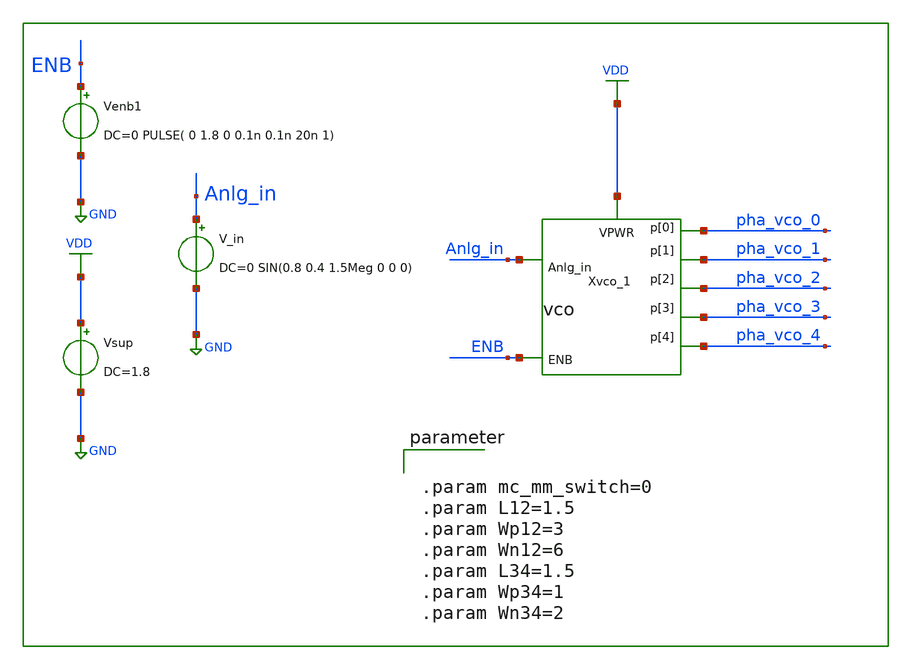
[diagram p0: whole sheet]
** sch_path: circuit_model/tb/vco.sch
**.subckt vco
Vsup VDD GND DC=1.8
V_in Anlg_in GND DC=0 SIN(0.8 0.4 1.5Meg 0 0 0)
Venb1 ENB GND DC=0 PULSE( 0 1.8 0 0.1n 0.1n 20n 1)
Xvco_1 VDD pha_vco_0 pha_vco_1 pha_vco_2 pha_vco_3 pha_vco_4 Anlg_in ENB vco L12="L12" Wp12="Wp12"
+ Wn12="Wn12" L34="L34" Wp34="Wp34" Wn34="Wn34"
**** begin user architecture code


.control
set nobreak
set num_threads=11
set test_mode = 0
* mode = 0: operation testing				1:  frequency extraction    2:  power consumption
if ($test_mode = 0)
    TRAN 1n 10u
    plot Anlg_in pha_vco_0
    MEAS TRAN prd_0 TRIG pha_vco_0 VAL=0.8 RISE=10 TARG pha_vco_0 VAL=0.8 RISE=20
    let freq_0 = 10/prd_0
    echo "frequency: "
    print freq_0
end

if ($test_mode = 1)
    let Vlow = 0
    let Vlimit = 1.01     $ set upper bound for sweeping
    let Vsweep = 0.2      $ set step size for sweeping
    let NoPoints=(Vlimit-Vlow)/Vsweep+2    $ set number of points for sweeping
    let freq_0 =unitvec(NoPoints)
    let Vin  =unitvec(NoPoints)
    let Vin[0]=Vlow
    let ix=0
    let I_vco =unitvec(NoPoints)
    while Vin[ix] < Vlimit
        alter V_in DC=Vin[ix]
        TRAN 1n 	10u
	SAVE @R_debug[i] pha_vco_0
        MEAS TRAN prd_0 TRIG pha_vco_0 VAL=0.8 RISE=10 TARG pha_vco_0 VAL=0.8 RISE =20
	MEAS TRAN Ivco 0 AVG @R_debug[i] FROM=1u TO=6u
	let I_vco[ix] = Ivco
        let freq_0[ix] = 10/prd_0
        let ix = ix+1
        Let Vin[ix] = Vin[ix-1]+Vsweep
    end
   print Vin freq_0 I_vco
end

if ($test_mode = 2)
    save "vdd" @Vsup[i] "p[0]"
    TRAN 1n 6u
    MEAS TRAN I_vco AVG @Vsup[i] FROM=3u TO=4u
    MEAS TRAN V_vco AVG vdd FROM=3u TO=4u
    let Power=I_vco*V_vco
    print Power
end
.endc




** Library on VNU server
.lib /home/dkits/efabless/mpw-5/pdks/sky130A/libs.tech/ngspice/sky130.lib.spice tt
.inc /home/dkits/efabless/mpw-5/pdks/sky130A/libs.ref/sky130_fd_sc_hd/spice/sky130_fd_sc_hd.spice
** Library on Home PC
*.lib /home/dkit/efabless/pdks/sky130A/libs.tech/ngspice/sky130.lib.spice tt
*.inc /home/dkit/efabless/pdks/sky130A/libs.ref/sky130_fd_sc_hd/spice/sky130_fd_sc_hd.spice




.param mc_mm_switch=0
.param L12=1.5
.param Wp12=3
.param Wn12=6
.param L34=1.5
.param Wp34=1
.param Wn34=2


**** end user architecture code
**.ends

* expanding   symbol:  /home/userdata/k63D/toind_63d/Desktop/project/circuit_model/lib/vco.sym # of
*+ pins=8
** sym_path: circuit_model/lib/vco.sym
** sch_path: circuit_model/lib/vco.sch
.subckt vco VPWR p[0] p[1] p[2] p[3] p[4] Anlg_in ENB  L12=0.15 Wp12=2.4 Wn12=1.2 L34=0.15 Wp34=1.2
+ Wn34=0.65
*.ipin Anlg_in
*.iopin VPWR
*.opin p[0]
*.ipin ENB
*.opin p[1]
*.opin p[2]
*.opin p[3]
*.opin p[4]
x1 VPWR ENB VGND VNB VPB VPWR pn[0] sky130_fd_sc_hd__einvp_1
Xro_1 Vctrl VPWR p[0] p[1] p[2] p[3] p[4] pn[0] pn[1] pn[2] pn[3] pn[4] ring_osc L12="L12"
+ Wp12="Wp12" Wn12="Wn12" L34="L34" Wp34="Wp34" Wn34="Wn34"
R2 Vctrl GND R=500 m=1
R1 Anlg_in Vctrl R=500 m=1
.ends


* expanding   symbol:  ring_osc.sym # of pins=12
** sym_path: circuit_model/lib/ring_osc.sym
** sch_path: circuit_model/lib/ring_osc.sch
.subckt ring_osc VGND VPWR p[0] p[1] p[2] p[3] p[4] pn[0] pn[1] pn[2] pn[3] pn[4]  L12=0.15 Wp12=2.4
+ Wn12=1.2 L34=0.15 Wp34=1.2 Wn34=0.65
*.iopin VPWR
*.iopin VGND
*.opin pn[0]
*.iopin p[0]
*.opin pn[1]
*.opin p[1]
*.opin p[2]
*.opin p[3]
*.opin p[4]
*.opin pn[2]
*.opin pn[3]
*.opin pn[4]
Xi_1 p[4] pn[4] VPWR VGND p[0] pn[0] cc_inv L12="L12" Wp12="Wp12" Wn12="Wn12" L34="L34" Wp34="Wp34"
+ Wn34="Wn34"
Xi_2 p[0] pn[0] VPWR VGND p[1] pn[1] cc_inv L12="L12" Wp12="Wp12" Wn12="Wn12" L34="L34" Wp34="Wp34"
+ Wn34="Wn34"
Xi_3 p[1] pn[1] VPWR VGND p[2] pn[2] cc_inv L12="L12" Wp12="Wp12" Wn12="Wn12" L34="L34" Wp34="Wp34"
+ Wn34="Wn34"
Xi_4 p[2] pn[2] VPWR VGND p[3] pn[3] cc_inv L12="L12" Wp12="Wp12" Wn12="Wn12" L34="L34" Wp34="Wp34"
+ Wn34="Wn34"
Xi_5 p[3] pn[3] VPWR VGND p[4] pn[4] cc_inv L12="L12" Wp12="Wp12" Wn12="Wn12" L34="L34" Wp34="Wp34"
+ Wn34="Wn34"
.ends


* expanding   symbol:  cc_inv.sym # of pins=6
** sym_path: circuit_model/lib/cc_inv.sym
** sch_path: circuit_model/lib/cc_inv.sch
.subckt cc_inv inp inn VPWR VGND outp outn  L12=0.15 Wp12=1.2 Wn12=0.65 L34=0.15 Wp34=1.2 Wn34=0.65
*.opin outp
*.ipin inn
*.iopin VGND
*.opin outn
*.ipin inp
*.iopin VPWR
Xi_1 inp VPWR VGND outp inverter L="L12" Wp="Wp12" Np=1 Wn="Wn12" Nn=1
Xi_3 outp VPWR VGND outn inverter L="L34" Wp="Wp34" Np=1 Wn="Wn34" Nn=1
Xi_2 inn VPWR VGND outn inverter L="L12" Wp="Wp12" Np=1 Wn="Wn12" Nn=1
Xi_4 outn VPWR VGND outp inverter L="L34" Wp="Wp34" Np=1 Wn="Wn34" Nn=1
.ends


* expanding   symbol:  inverter.sym # of pins=4
** sym_path: circuit_model/lib/inverter.sym
** sch_path: circuit_model/lib/inverter.sch
.subckt inverter A VPWR VGND Y  L=0.15 Wp=1.2 Np=1 Wn=0.65 Nn=1
*.iopin VPWR
*.iopin VGND
*.ipin A
*.opin Y
XM1 Y A VPWR VDD sky130_fd_pr__pfet_01v8 L="L" W="Wp" nf="Np" ad='int(("Np" + 1)/2) * "Wp" / "Np" * 0.29'
+ as='int(("Np" + 2)/2) * "Wp" / "Np" * 0.29' pd='2*int(("Np" + 1)/2) * ("Wp" / "Np" + 0.29)' ps='2*int(("Np" + 2)/2) * ("Wp" / "Np" + 0.29)'
+ nrd='0.29 / "Wp" ' nrs='0.29 / "Wp" ' sa=0 sb=0 sd=0 mult=1 m=1
XM2 Y A VGND GND sky130_fd_pr__nfet_01v8 L="L" W="Wn" nf="Nn" ad='int((nf+1)/2) * W/nf * 0.29' as='int((nf+2)/2) * W/nf * 0.29'
+ pd='2*int((nf+1)/2) * (W/nf + 0.29)' ps='2*int((nf+2)/2) * (W/nf + 0.29)' nrd='0.29 / W' nrs='0.29 / W'
+ sa=0 sb=0 sd=0 mult=1 m=1
.ends

.GLOBAL VDD
.GLOBAL GND
.end
